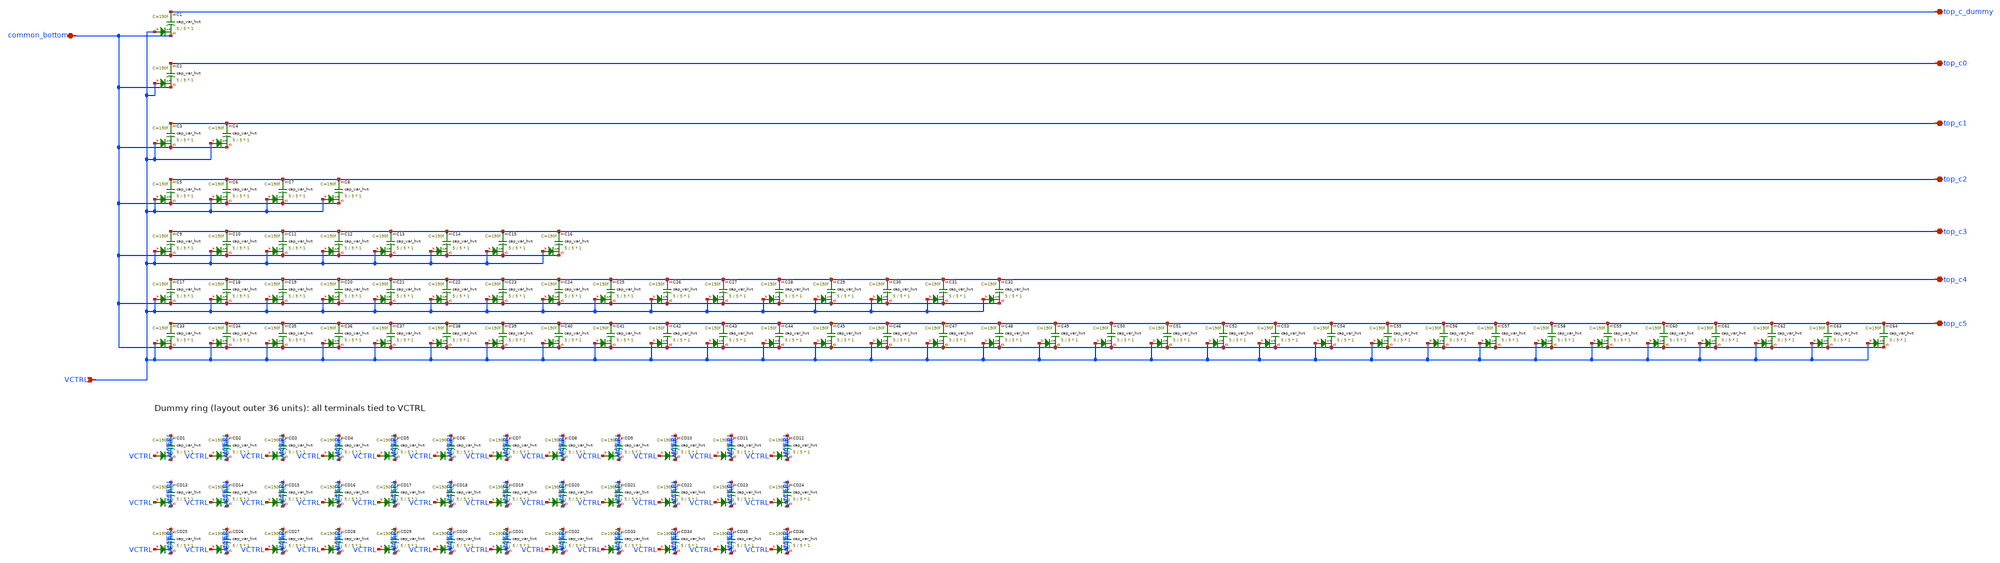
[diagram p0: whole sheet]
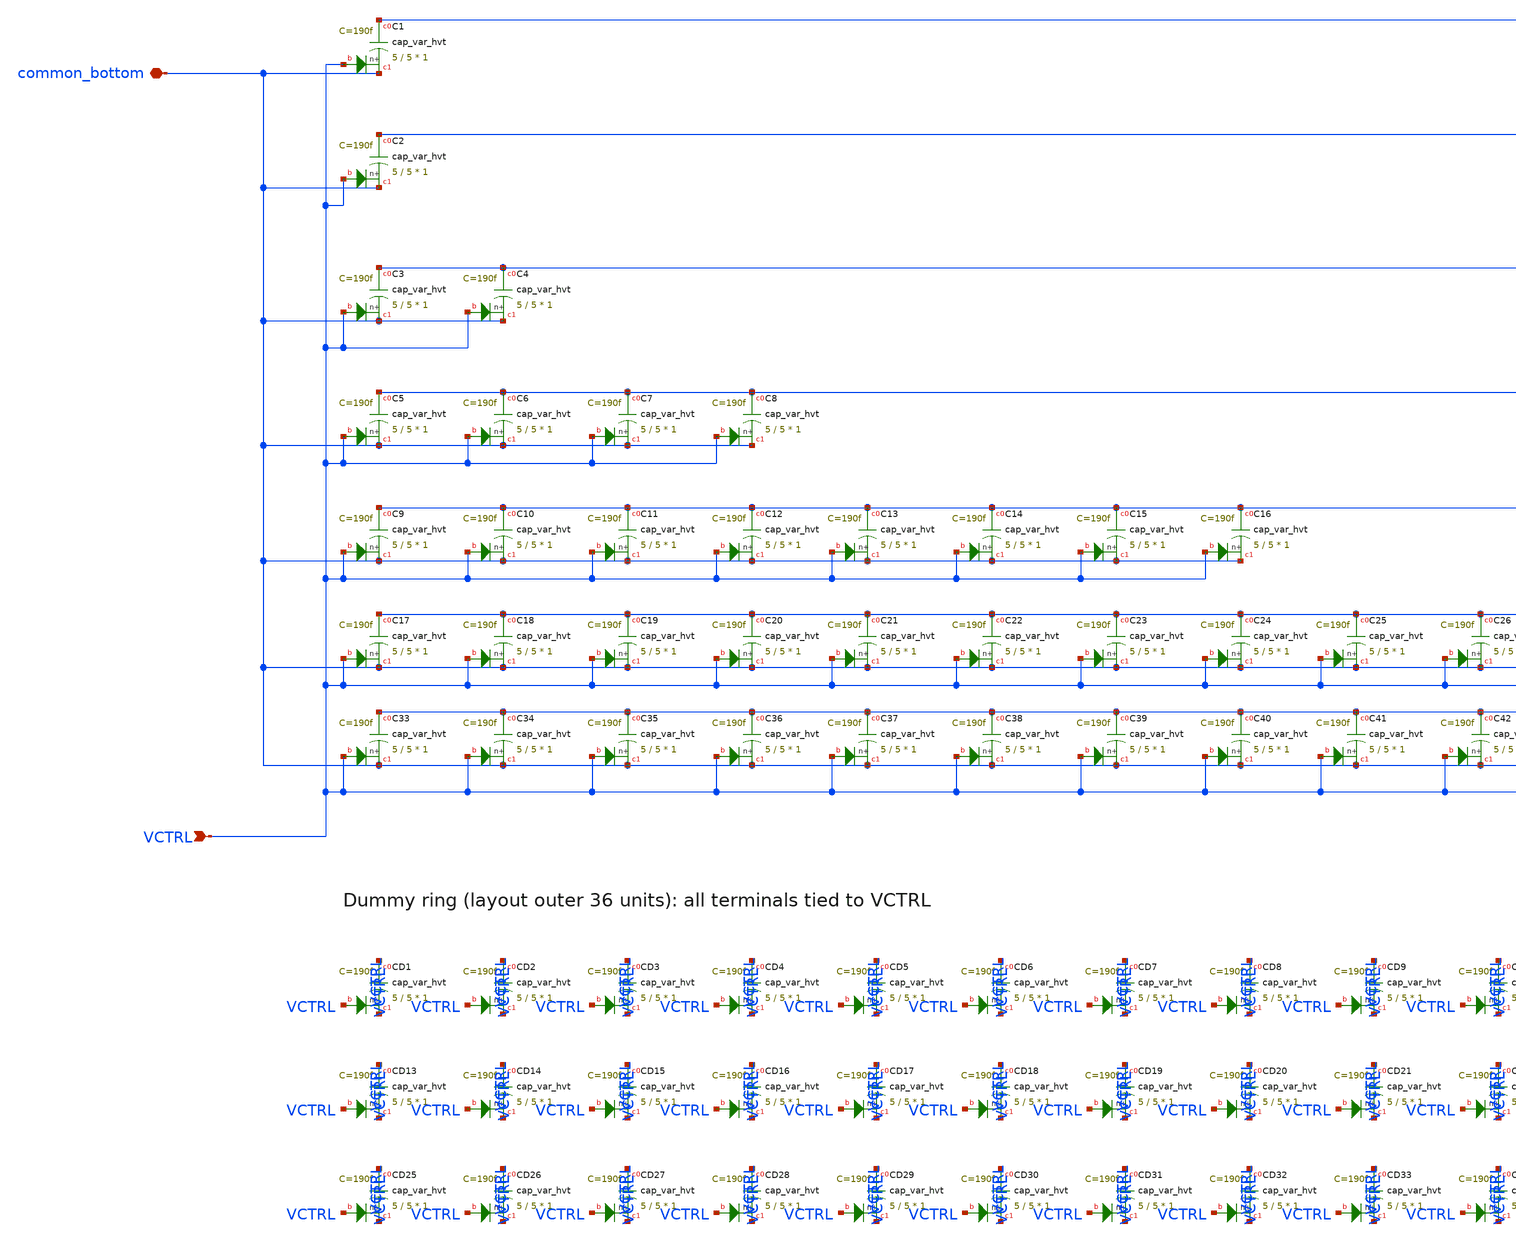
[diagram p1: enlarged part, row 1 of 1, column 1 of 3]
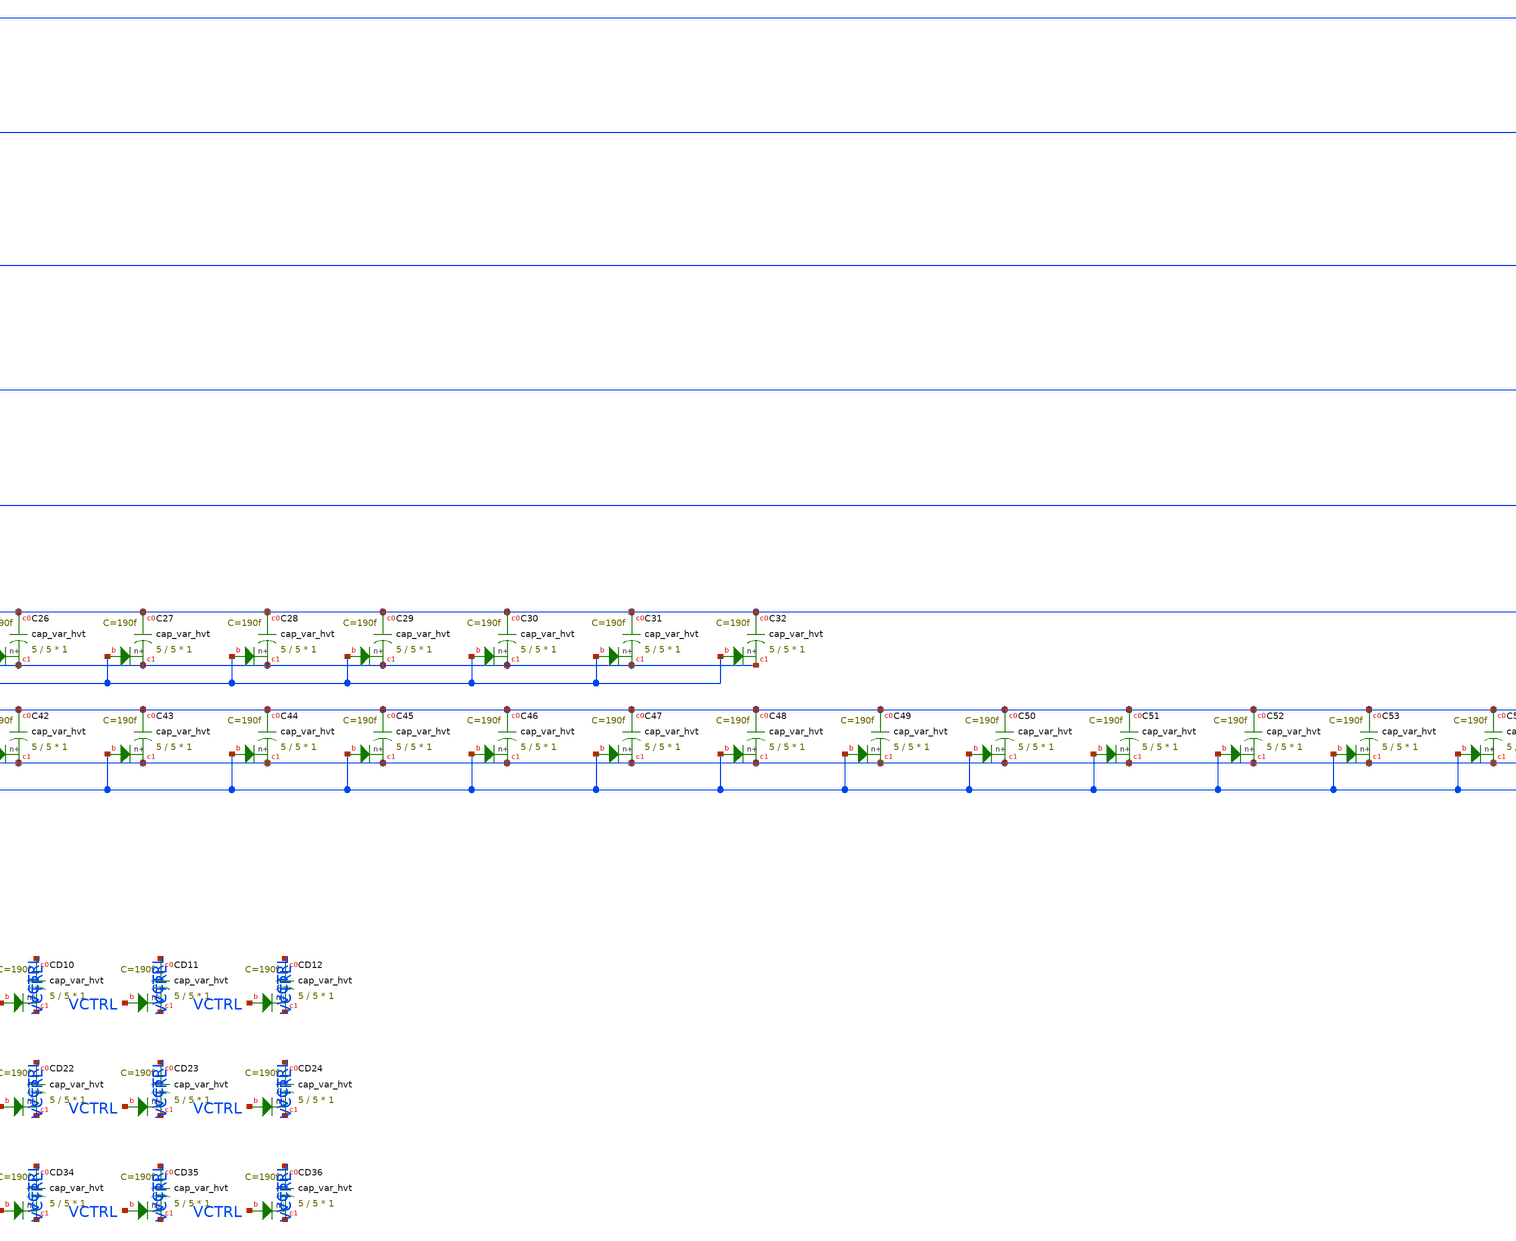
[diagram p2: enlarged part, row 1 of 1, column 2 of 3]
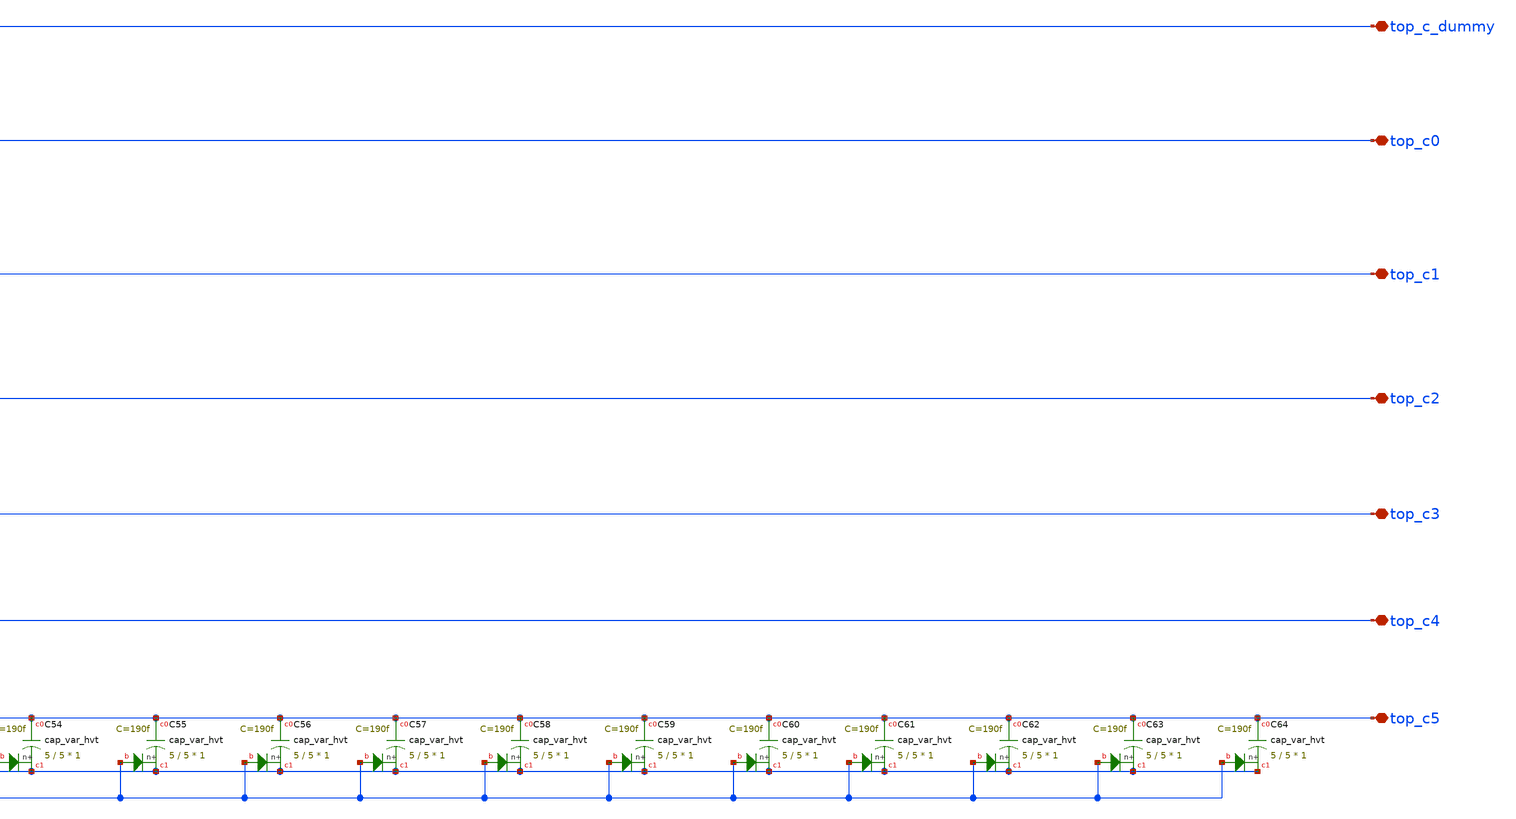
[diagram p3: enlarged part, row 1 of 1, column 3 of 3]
** sch_path: xschem/cap_array_var.sch
**.subckt cap_array_var common_bottom top_c_dummy top_c0 top_c5 top_c4 top_c3 top_c2 top_c1 VCTRL
*.iopin common_bottom
*.iopin top_c_dummy
*.iopin top_c0
*.iopin top_c5
*.iopin top_c4
*.iopin top_c3
*.iopin top_c2
*.iopin top_c1
*.ipin VCTRL
XC1 top_c_dummy common_bottom VCTRL sky130_fd_pr__cap_var_hvt W=5 L=5 VM=1 m=1
XC2 top_c0 common_bottom VCTRL sky130_fd_pr__cap_var_hvt W=5 L=5 VM=1 m=1
XC3 top_c1 common_bottom VCTRL sky130_fd_pr__cap_var_hvt W=5 L=5 VM=1 m=1
XC4 top_c1 common_bottom VCTRL sky130_fd_pr__cap_var_hvt W=5 L=5 VM=1 m=1
XC5 top_c2 common_bottom VCTRL sky130_fd_pr__cap_var_hvt W=5 L=5 VM=1 m=1
XC6 top_c2 common_bottom VCTRL sky130_fd_pr__cap_var_hvt W=5 L=5 VM=1 m=1
XC7 top_c2 common_bottom VCTRL sky130_fd_pr__cap_var_hvt W=5 L=5 VM=1 m=1
XC8 top_c2 common_bottom VCTRL sky130_fd_pr__cap_var_hvt W=5 L=5 VM=1 m=1
XC9 top_c3 common_bottom VCTRL sky130_fd_pr__cap_var_hvt W=5 L=5 VM=1 m=1
XC10 top_c3 common_bottom VCTRL sky130_fd_pr__cap_var_hvt W=5 L=5 VM=1 m=1
XC11 top_c3 common_bottom VCTRL sky130_fd_pr__cap_var_hvt W=5 L=5 VM=1 m=1
XC12 top_c3 common_bottom VCTRL sky130_fd_pr__cap_var_hvt W=5 L=5 VM=1 m=1
XC13 top_c3 common_bottom VCTRL sky130_fd_pr__cap_var_hvt W=5 L=5 VM=1 m=1
XC14 top_c3 common_bottom VCTRL sky130_fd_pr__cap_var_hvt W=5 L=5 VM=1 m=1
XC15 top_c3 common_bottom VCTRL sky130_fd_pr__cap_var_hvt W=5 L=5 VM=1 m=1
XC16 top_c3 common_bottom VCTRL sky130_fd_pr__cap_var_hvt W=5 L=5 VM=1 m=1
XC17 top_c4 common_bottom VCTRL sky130_fd_pr__cap_var_hvt W=5 L=5 VM=1 m=1
XC18 top_c4 common_bottom VCTRL sky130_fd_pr__cap_var_hvt W=5 L=5 VM=1 m=1
XC19 top_c4 common_bottom VCTRL sky130_fd_pr__cap_var_hvt W=5 L=5 VM=1 m=1
XC20 top_c4 common_bottom VCTRL sky130_fd_pr__cap_var_hvt W=5 L=5 VM=1 m=1
XC21 top_c4 common_bottom VCTRL sky130_fd_pr__cap_var_hvt W=5 L=5 VM=1 m=1
XC22 top_c4 common_bottom VCTRL sky130_fd_pr__cap_var_hvt W=5 L=5 VM=1 m=1
XC23 top_c4 common_bottom VCTRL sky130_fd_pr__cap_var_hvt W=5 L=5 VM=1 m=1
XC24 top_c4 common_bottom VCTRL sky130_fd_pr__cap_var_hvt W=5 L=5 VM=1 m=1
XC25 top_c4 common_bottom VCTRL sky130_fd_pr__cap_var_hvt W=5 L=5 VM=1 m=1
XC26 top_c4 common_bottom VCTRL sky130_fd_pr__cap_var_hvt W=5 L=5 VM=1 m=1
XC27 top_c4 common_bottom VCTRL sky130_fd_pr__cap_var_hvt W=5 L=5 VM=1 m=1
XC28 top_c4 common_bottom VCTRL sky130_fd_pr__cap_var_hvt W=5 L=5 VM=1 m=1
XC29 top_c4 common_bottom VCTRL sky130_fd_pr__cap_var_hvt W=5 L=5 VM=1 m=1
XC30 top_c4 common_bottom VCTRL sky130_fd_pr__cap_var_hvt W=5 L=5 VM=1 m=1
XC31 top_c4 common_bottom VCTRL sky130_fd_pr__cap_var_hvt W=5 L=5 VM=1 m=1
XC32 top_c4 common_bottom VCTRL sky130_fd_pr__cap_var_hvt W=5 L=5 VM=1 m=1
XC33 top_c5 common_bottom VCTRL sky130_fd_pr__cap_var_hvt W=5 L=5 VM=1 m=1
XC34 top_c5 common_bottom VCTRL sky130_fd_pr__cap_var_hvt W=5 L=5 VM=1 m=1
XC35 top_c5 common_bottom VCTRL sky130_fd_pr__cap_var_hvt W=5 L=5 VM=1 m=1
XC36 top_c5 common_bottom VCTRL sky130_fd_pr__cap_var_hvt W=5 L=5 VM=1 m=1
XC37 top_c5 common_bottom VCTRL sky130_fd_pr__cap_var_hvt W=5 L=5 VM=1 m=1
XC38 top_c5 common_bottom VCTRL sky130_fd_pr__cap_var_hvt W=5 L=5 VM=1 m=1
XC39 top_c5 common_bottom VCTRL sky130_fd_pr__cap_var_hvt W=5 L=5 VM=1 m=1
XC40 top_c5 common_bottom VCTRL sky130_fd_pr__cap_var_hvt W=5 L=5 VM=1 m=1
XC41 top_c5 common_bottom VCTRL sky130_fd_pr__cap_var_hvt W=5 L=5 VM=1 m=1
XC42 top_c5 common_bottom VCTRL sky130_fd_pr__cap_var_hvt W=5 L=5 VM=1 m=1
XC43 top_c5 common_bottom VCTRL sky130_fd_pr__cap_var_hvt W=5 L=5 VM=1 m=1
XC44 top_c5 common_bottom VCTRL sky130_fd_pr__cap_var_hvt W=5 L=5 VM=1 m=1
XC45 top_c5 common_bottom VCTRL sky130_fd_pr__cap_var_hvt W=5 L=5 VM=1 m=1
XC46 top_c5 common_bottom VCTRL sky130_fd_pr__cap_var_hvt W=5 L=5 VM=1 m=1
XC47 top_c5 common_bottom VCTRL sky130_fd_pr__cap_var_hvt W=5 L=5 VM=1 m=1
XC48 top_c5 common_bottom VCTRL sky130_fd_pr__cap_var_hvt W=5 L=5 VM=1 m=1
XC49 top_c5 common_bottom VCTRL sky130_fd_pr__cap_var_hvt W=5 L=5 VM=1 m=1
XC50 top_c5 common_bottom VCTRL sky130_fd_pr__cap_var_hvt W=5 L=5 VM=1 m=1
XC51 top_c5 common_bottom VCTRL sky130_fd_pr__cap_var_hvt W=5 L=5 VM=1 m=1
XC52 top_c5 common_bottom VCTRL sky130_fd_pr__cap_var_hvt W=5 L=5 VM=1 m=1
XC53 top_c5 common_bottom VCTRL sky130_fd_pr__cap_var_hvt W=5 L=5 VM=1 m=1
XC54 top_c5 common_bottom VCTRL sky130_fd_pr__cap_var_hvt W=5 L=5 VM=1 m=1
XC55 top_c5 common_bottom VCTRL sky130_fd_pr__cap_var_hvt W=5 L=5 VM=1 m=1
XC56 top_c5 common_bottom VCTRL sky130_fd_pr__cap_var_hvt W=5 L=5 VM=1 m=1
XC57 top_c5 common_bottom VCTRL sky130_fd_pr__cap_var_hvt W=5 L=5 VM=1 m=1
XC58 top_c5 common_bottom VCTRL sky130_fd_pr__cap_var_hvt W=5 L=5 VM=1 m=1
XC59 top_c5 common_bottom VCTRL sky130_fd_pr__cap_var_hvt W=5 L=5 VM=1 m=1
XC60 top_c5 common_bottom VCTRL sky130_fd_pr__cap_var_hvt W=5 L=5 VM=1 m=1
XC61 top_c5 common_bottom VCTRL sky130_fd_pr__cap_var_hvt W=5 L=5 VM=1 m=1
XC62 top_c5 common_bottom VCTRL sky130_fd_pr__cap_var_hvt W=5 L=5 VM=1 m=1
XC63 top_c5 common_bottom VCTRL sky130_fd_pr__cap_var_hvt W=5 L=5 VM=1 m=1
XC64 top_c5 common_bottom VCTRL sky130_fd_pr__cap_var_hvt W=5 L=5 VM=1 m=1
XCD1 VCTRL VCTRL VCTRL sky130_fd_pr__cap_var_hvt W=5 L=5 VM=1 m=1
XCD2 VCTRL VCTRL VCTRL sky130_fd_pr__cap_var_hvt W=5 L=5 VM=1 m=1
XCD3 VCTRL VCTRL VCTRL sky130_fd_pr__cap_var_hvt W=5 L=5 VM=1 m=1
XCD4 VCTRL VCTRL VCTRL sky130_fd_pr__cap_var_hvt W=5 L=5 VM=1 m=1
XCD5 VCTRL VCTRL VCTRL sky130_fd_pr__cap_var_hvt W=5 L=5 VM=1 m=1
XCD6 VCTRL VCTRL VCTRL sky130_fd_pr__cap_var_hvt W=5 L=5 VM=1 m=1
XCD7 VCTRL VCTRL VCTRL sky130_fd_pr__cap_var_hvt W=5 L=5 VM=1 m=1
XCD8 VCTRL VCTRL VCTRL sky130_fd_pr__cap_var_hvt W=5 L=5 VM=1 m=1
XCD9 VCTRL VCTRL VCTRL sky130_fd_pr__cap_var_hvt W=5 L=5 VM=1 m=1
XCD10 VCTRL VCTRL VCTRL sky130_fd_pr__cap_var_hvt W=5 L=5 VM=1 m=1
XCD11 VCTRL VCTRL VCTRL sky130_fd_pr__cap_var_hvt W=5 L=5 VM=1 m=1
XCD12 VCTRL VCTRL VCTRL sky130_fd_pr__cap_var_hvt W=5 L=5 VM=1 m=1
XCD13 VCTRL VCTRL VCTRL sky130_fd_pr__cap_var_hvt W=5 L=5 VM=1 m=1
XCD14 VCTRL VCTRL VCTRL sky130_fd_pr__cap_var_hvt W=5 L=5 VM=1 m=1
XCD15 VCTRL VCTRL VCTRL sky130_fd_pr__cap_var_hvt W=5 L=5 VM=1 m=1
XCD16 VCTRL VCTRL VCTRL sky130_fd_pr__cap_var_hvt W=5 L=5 VM=1 m=1
XCD17 VCTRL VCTRL VCTRL sky130_fd_pr__cap_var_hvt W=5 L=5 VM=1 m=1
XCD18 VCTRL VCTRL VCTRL sky130_fd_pr__cap_var_hvt W=5 L=5 VM=1 m=1
XCD19 VCTRL VCTRL VCTRL sky130_fd_pr__cap_var_hvt W=5 L=5 VM=1 m=1
XCD20 VCTRL VCTRL VCTRL sky130_fd_pr__cap_var_hvt W=5 L=5 VM=1 m=1
XCD21 VCTRL VCTRL VCTRL sky130_fd_pr__cap_var_hvt W=5 L=5 VM=1 m=1
XCD22 VCTRL VCTRL VCTRL sky130_fd_pr__cap_var_hvt W=5 L=5 VM=1 m=1
XCD23 VCTRL VCTRL VCTRL sky130_fd_pr__cap_var_hvt W=5 L=5 VM=1 m=1
XCD24 VCTRL VCTRL VCTRL sky130_fd_pr__cap_var_hvt W=5 L=5 VM=1 m=1
XCD25 VCTRL VCTRL VCTRL sky130_fd_pr__cap_var_hvt W=5 L=5 VM=1 m=1
XCD26 VCTRL VCTRL VCTRL sky130_fd_pr__cap_var_hvt W=5 L=5 VM=1 m=1
XCD27 VCTRL VCTRL VCTRL sky130_fd_pr__cap_var_hvt W=5 L=5 VM=1 m=1
XCD28 VCTRL VCTRL VCTRL sky130_fd_pr__cap_var_hvt W=5 L=5 VM=1 m=1
XCD29 VCTRL VCTRL VCTRL sky130_fd_pr__cap_var_hvt W=5 L=5 VM=1 m=1
XCD30 VCTRL VCTRL VCTRL sky130_fd_pr__cap_var_hvt W=5 L=5 VM=1 m=1
XCD31 VCTRL VCTRL VCTRL sky130_fd_pr__cap_var_hvt W=5 L=5 VM=1 m=1
XCD32 VCTRL VCTRL VCTRL sky130_fd_pr__cap_var_hvt W=5 L=5 VM=1 m=1
XCD33 VCTRL VCTRL VCTRL sky130_fd_pr__cap_var_hvt W=5 L=5 VM=1 m=1
XCD34 VCTRL VCTRL VCTRL sky130_fd_pr__cap_var_hvt W=5 L=5 VM=1 m=1
XCD35 VCTRL VCTRL VCTRL sky130_fd_pr__cap_var_hvt W=5 L=5 VM=1 m=1
XCD36 VCTRL VCTRL VCTRL sky130_fd_pr__cap_var_hvt W=5 L=5 VM=1 m=1
**.ends
.end
